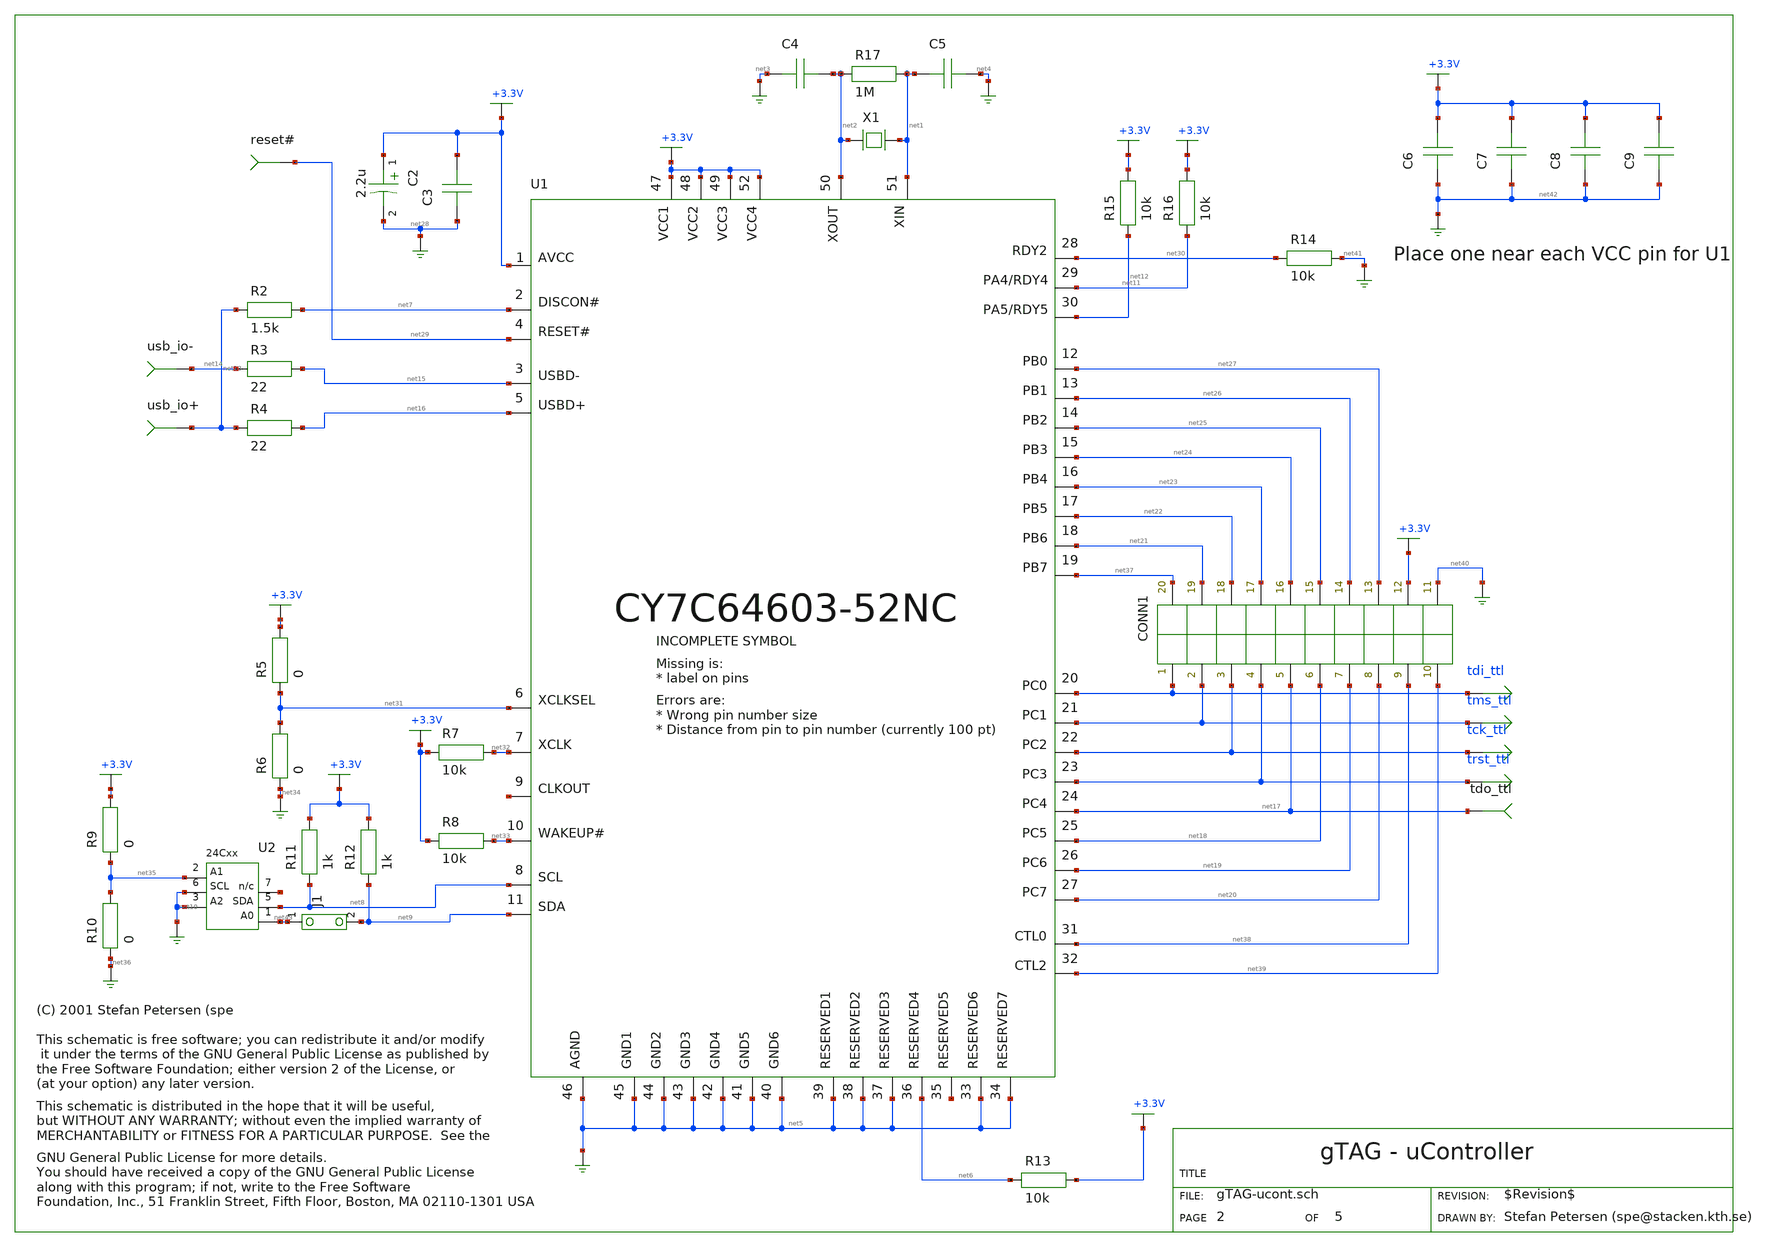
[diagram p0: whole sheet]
** sch_path: xschem_library/gschem_import/gTAG-ucont.sch
* copyleft.sym
**.subckt gTAG-ucont tdi_ttl tms_ttl tck_ttl trst_ttl
U2 net35 net10 net10 net43 net8 net44 Vcc GND
X1 net2 net1 12MHz
R17 net2 net1 1M
C4 net3 net2 30p
C5 net1 net4 30p
R13 net6 +3.3V 10k
usb_io+ net13
usb_io- net14
R2 net13 net7 1.5k
R12 net9 +3.3V 1k
R11 net8 +3.3V 1k
R6 net34 net31 0
R15 net12 +3.3V 10k
R4 net13 net16 22
R3 net14 net15 22
R5 net31 +3.3V 0
R7 +3.3V net32 10k
R8 +3.3V net33 10k
C3 net28 +3.3V 100n
C2 +3.3V net28 2.2u
U1 +3.3V net8 net9 net33 +3.3V net1 net2 net5 net5 net11 net12 net45 net5 +3.3V net5 net31 net5 net7
+ net6 net46 net5 net5 net5 net15 net16 net5 +3.3V net29 net27 net26 net25 net24 net23 net22 net21 net37
+ net39 net32 net5 +3.3V net38 net30 tdi_ttl tms_ttl tck_ttl trst_ttl net5 net17 net18 net19 net20 net5
tdo_ttl net17
R16 net11 +3.3V 10k
R14 net30 net41 10k
R10 net36 net35 0
R9 net35 +3.3V 0
C6 net42 +3.3V 100n
C7 net42 +3.3V 100n
C8 net42 +3.3V 100n
C9 net42 +3.3V 100n
J1 net9 net43
reset# net29
CONN1 tdi_ttl tms_ttl tck_ttl trst_ttl net17 net18 net19 net20 net38 net39 net40 +3.3V net27 net26
+ net25 net24 net23 net22 net21 net37
**.ends
.end
